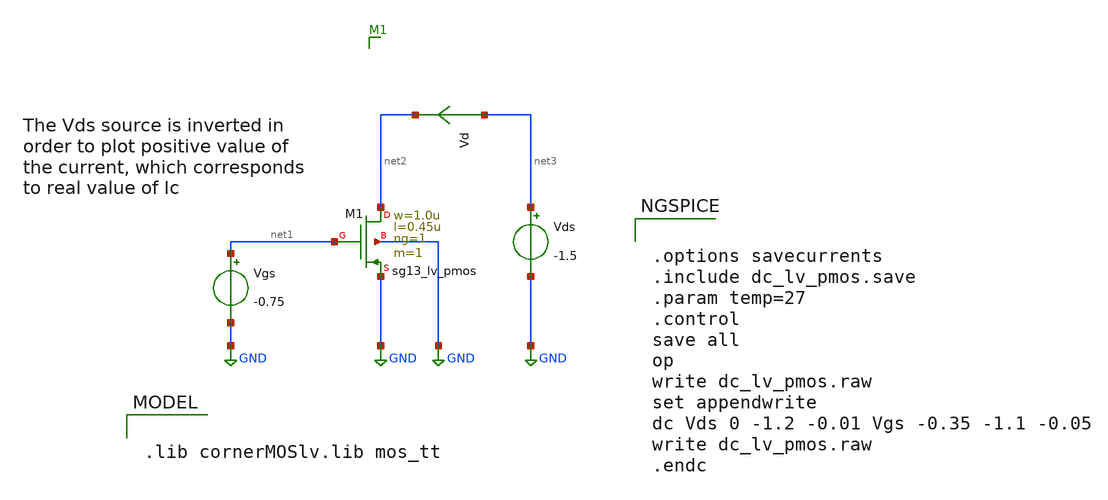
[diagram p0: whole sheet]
** sch_path: ihp-sg13g2/libs.tech/xschem/sg13g2_tests/dc_lv_pmos.sch
* Copyright 2023 IHP PDK Authors
**.subckt dc_lv_pmos
Vgs net1 GND -0.75
Vds net3 GND -1.5
Vd net3 net2 0
.save i(vd)
XM1 GND net1 net2 GND sg13_lv_pmos w=1.0u l=0.45u ng=1 m=1
**** begin user architecture code

.lib cornerMOSlv.lib mos_tt



.options savecurrents
.include dc_lv_pmos.save
.param temp=27
.control
save all
op
write dc_lv_pmos.raw
set appendwrite
dc Vds 0 -1.2 -0.01 Vgs -0.35 -1.1 -0.05
write dc_lv_pmos.raw
.endc


**** end user architecture code
**.ends
.GLOBAL GND
.end
